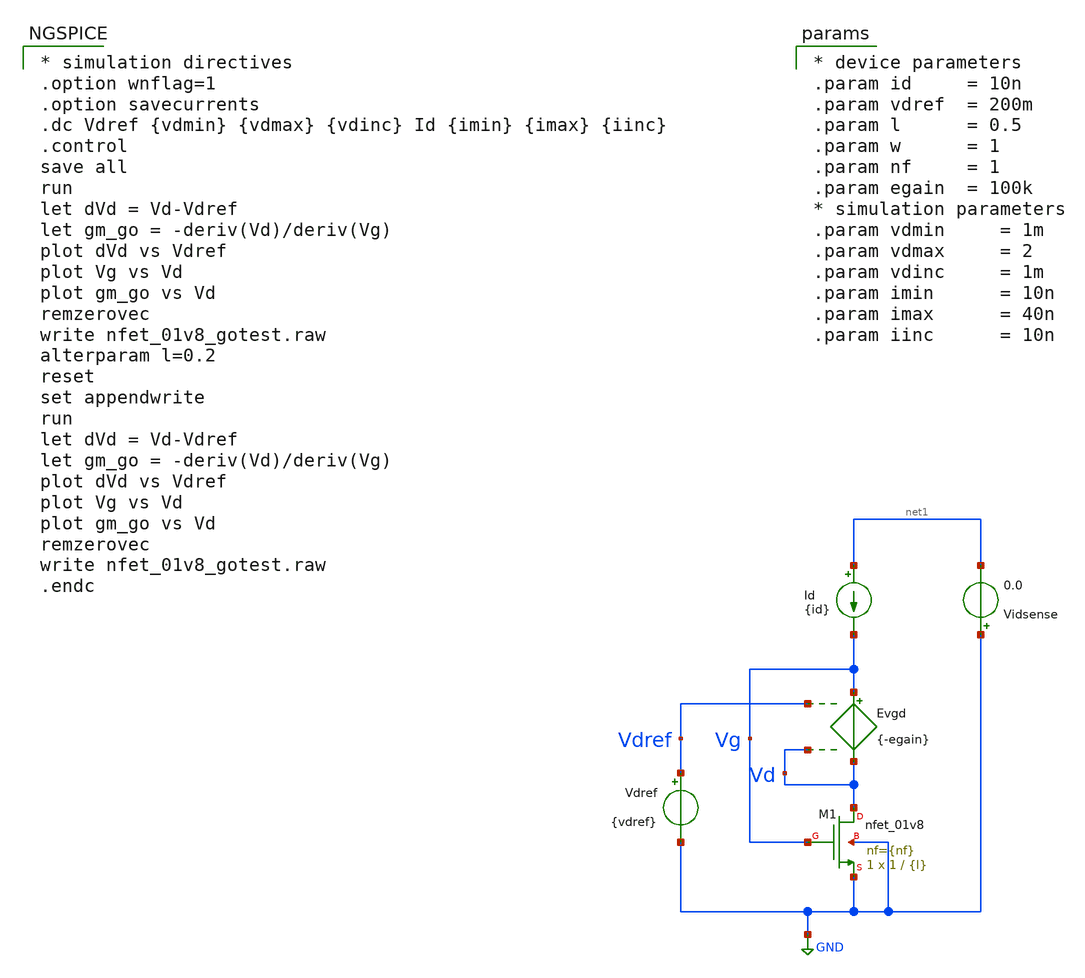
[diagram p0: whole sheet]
** sch_path: xschem/nfet_01v8_gotest.sch
**.subckt nfet_01v8_gotest
Evgd Vg Vd Vdref Vd {-egain}
Id net1 Vg {id}
Vdref Vdref GND {vdref}
Vidsense GND net1 0.0
XM1 Vd Vg GND GND sky130_fd_pr__nfet_01v8 L={l} W=1 nf={nf} ad='int((nf+1)/2) * W/nf * 0.29' as='int((nf+2)/2) * W/nf * 0.29'
+ pd='2*int((nf+1)/2) * (W/nf + 0.29)' ps='2*int((nf+2)/2) * (W/nf + 0.29)' nrd='0.29 / W' nrs='0.29 / W'
+ sa=0 sb=0 sd=0 mult=1 m=1
**** begin user architecture code

** opencircuitdesign pdks install
.lib $::SKYWATER_MODELS/sky130.lib.spice tt



* simulation directives
.option wnflag=1
.option savecurrents
.dc Vdref {vdmin} {vdmax} {vdinc} Id {imin} {imax} {iinc}
.control
save all
run
let dVd = Vd-Vdref
let gm_go = -deriv(Vd)/deriv(Vg)
plot dVd vs Vdref
plot Vg vs Vd
plot gm_go vs Vd
remzerovec
write nfet_01v8_gotest.raw
alterparam l=0.2
reset
set appendwrite
run
let dVd = Vd-Vdref
let gm_go = -deriv(Vd)/deriv(Vg)
plot dVd vs Vdref
plot Vg vs Vd
plot gm_go vs Vd
remzerovec
write nfet_01v8_gotest.raw
.endc



* device parameters
.param id     = 10n
.param vdref  = 200m
.param l      = 0.5
.param w      = 1
.param nf     = 1
.param egain  = 100k
* simulation parameters
.param vdmin     = 1m
.param vdmax     = 2
.param vdinc     = 1m
.param imin      = 10n
.param imax      = 40n
.param iinc      = 10n


**** end user architecture code
**.ends
.GLOBAL GND
.end
